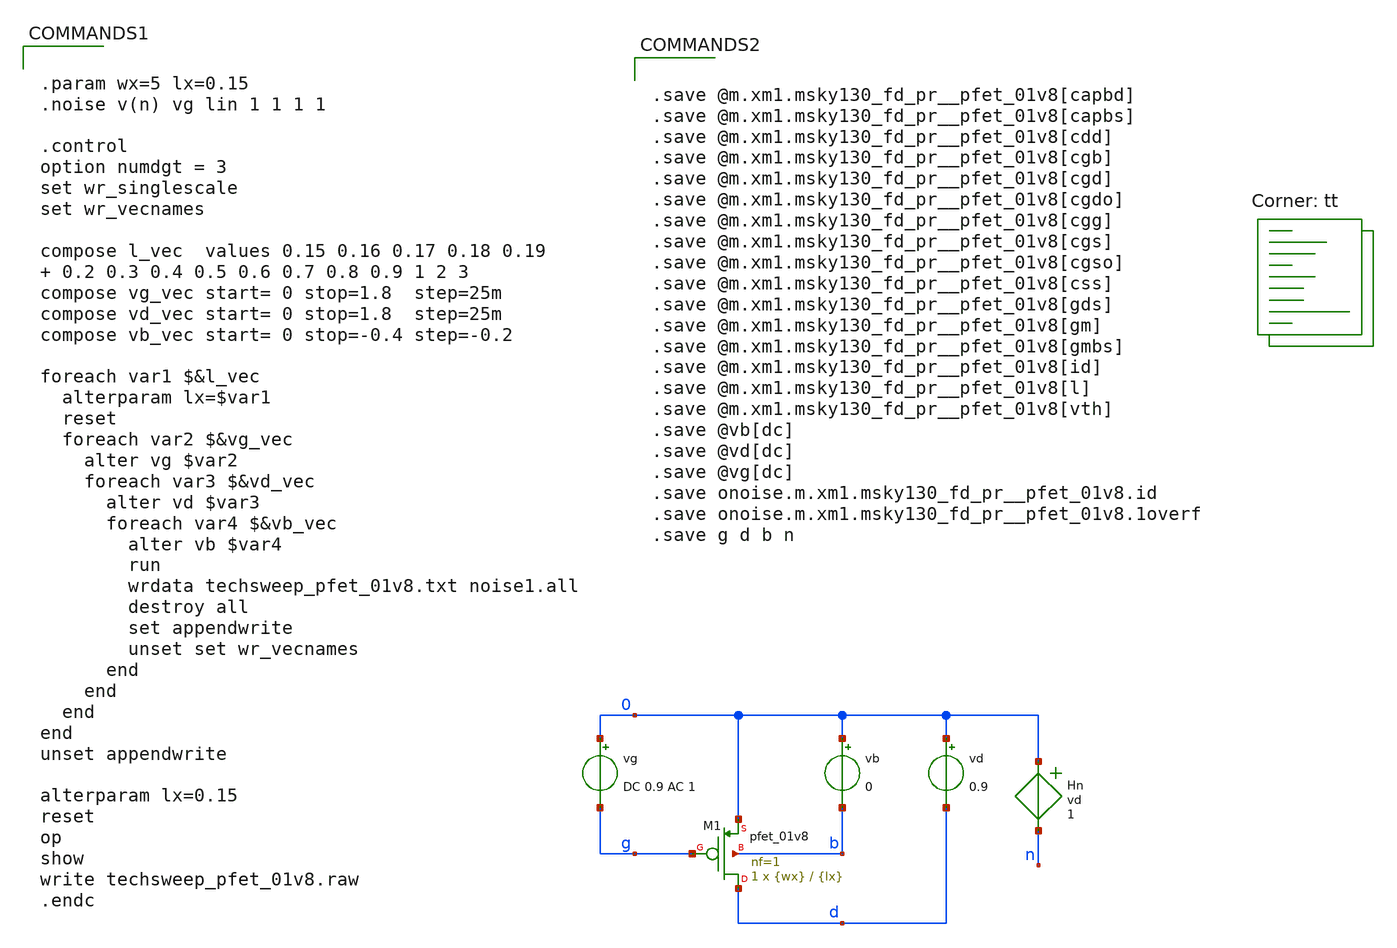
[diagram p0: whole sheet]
** sch_path: projects/bandgapref/xschem_ngspice/new_files/technology_parameter_check/starter_files_open_source_tools/sky130/techsweep_pfet_01v8.sch
**.subckt techsweep_pfet_01v8
Hn 0 n vd 1
vg 0 g DC 0.9 AC 1
vd 0 d 0.9
vb 0 b 0
XM1 d g 0 b sky130_fd_pr__pfet_01v8 L={lx} W={wx} nf=1 ad='int((nf+1)/2) * W/nf * 0.29' as='int((nf+2)/2) * W/nf * 0.29'
+ pd='2*int((nf+1)/2) * (W/nf + 0.29)' ps='2*int((nf+2)/2) * (W/nf + 0.29)' nrd='0.29 / W' nrs='0.29 / W'
+ sa=0 sb=0 sd=0 mult=1 m=1
**** begin user architecture code


.param wx=5 lx=0.15
.noise v(n) vg lin 1 1 1 1

.control
option numdgt = 3
set wr_singlescale
set wr_vecnames

compose l_vec  values 0.15 0.16 0.17 0.18 0.19  0.2 0.3 0.4 0.5 0.6 0.7 0.8 0.9 1 2 3
compose vg_vec start= 0 stop=1.8  step=25m
compose vd_vec start= 0 stop=1.8  step=25m
compose vb_vec start= 0 stop=-0.4 step=-0.2

foreach var1 $&l_vec
  alterparam lx=$var1
  reset
  foreach var2 $&vg_vec
    alter vg $var2
    foreach var3 $&vd_vec
      alter vd $var3
      foreach var4 $&vb_vec
        alter vb $var4
        run
        wrdata techsweep_pfet_01v8.txt noise1.all
        destroy all
        set appendwrite
        unset set wr_vecnames
      end
    end
  end
end
unset appendwrite

alterparam lx=0.15
reset
op
show
write techsweep_pfet_01v8.raw
.endc


.lib $::SKYWATER_MODELS/sky130.lib.spice tt


.save @m.xm1.msky130_fd_pr__pfet_01v8[capbd]
.save @m.xm1.msky130_fd_pr__pfet_01v8[capbs]
.save @m.xm1.msky130_fd_pr__pfet_01v8[cdd]
.save @m.xm1.msky130_fd_pr__pfet_01v8[cgb]
.save @m.xm1.msky130_fd_pr__pfet_01v8[cgd]
.save @m.xm1.msky130_fd_pr__pfet_01v8[cgdo]
.save @m.xm1.msky130_fd_pr__pfet_01v8[cgg]
.save @m.xm1.msky130_fd_pr__pfet_01v8[cgs]
.save @m.xm1.msky130_fd_pr__pfet_01v8[cgso]
.save @m.xm1.msky130_fd_pr__pfet_01v8[css]
.save @m.xm1.msky130_fd_pr__pfet_01v8[gds]
.save @m.xm1.msky130_fd_pr__pfet_01v8[gm]
.save @m.xm1.msky130_fd_pr__pfet_01v8[gmbs]
.save @m.xm1.msky130_fd_pr__pfet_01v8[id]
.save @m.xm1.msky130_fd_pr__pfet_01v8[l]
.save @m.xm1.msky130_fd_pr__pfet_01v8[vth]
.save @vb[dc]
.save @vd[dc]
.save @vg[dc]
.save onoise.m.xm1.msky130_fd_pr__pfet_01v8.id
.save onoise.m.xm1.msky130_fd_pr__pfet_01v8.1overf
.save g d b n


**** end user architecture code
**.ends
.end
